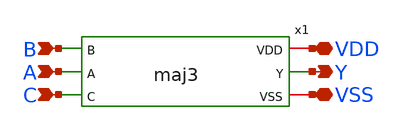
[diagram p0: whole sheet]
** sch_path: xschem/simulate.sch
**.subckt simulate A B C Y VDD VSS
*.ipin A
*.ipin B
*.ipin C
*.opin Y
*.iopin VDD
*.iopin VSS
x1 VDD B A C Y VSS maj3
**** begin user architecture code

.lib /foss/pdks/gf180mcuD/libs.tech/ngspice/sm141064.ngspice typical
.param fnoicor=1
.param sw_stat_mismatch=0
V1 VDD GND 3.3
V2 VSS GND 0
V3 A GND PULSE(0 3.3 10n 100p 100p 10n 20n)
V4 B GND PULSE(0 3.3 0 100p 100p 20n 40n)
V5 C GND PULSE(0 3.3 0 100p 100p 40n 80n)
.tran 10p 100n
.control
set filetype=ascii
run
write simulate.raw
plot v(A)-7 v(B)-3.5 v(C) v(Y)+3.5
.endc

**** end user architecture code
**.ends

* expanding   symbol:  maj3.sym # of pins=6
** sym_path: xschem/maj3.sym
** sch_path: xschem/maj3.sch
.subckt maj3 VDD B A C Y VSS
*.ipin A
*.ipin C
*.ipin B
*.opin Y
*.iopin VDD
*.iopin VSS
XM1 net1 A VDD VDD pfet_03v3 L=0.28u W=0.22u nf=1 ad='int((nf+1)/2) * W/nf * 0.18u' as='int((nf+2)/2) * W/nf * 0.18u'
+ pd='2*int((nf+1)/2) * (W/nf + 0.18u)' ps='2*int((nf+2)/2) * (W/nf + 0.18u)' nrd='0.18u / W' nrs='0.18u / W'
+ sa=0 sb=0 sd=0 m=1
XM2 X C net1 VDD pfet_03v3 L=0.28u W=0.22u nf=1 ad='int((nf+1)/2) * W/nf * 0.18u' as='int((nf+2)/2) * W/nf * 0.18u'
+ pd='2*int((nf+1)/2) * (W/nf + 0.18u)' ps='2*int((nf+2)/2) * (W/nf + 0.18u)' nrd='0.18u / W' nrs='0.18u / W'
+ sa=0 sb=0 sd=0 m=1
XM3 net2 B VDD VDD pfet_03v3 L=0.28u W=0.22u nf=1 ad='int((nf+1)/2) * W/nf * 0.18u' as='int((nf+2)/2) * W/nf * 0.18u'
+ pd='2*int((nf+1)/2) * (W/nf + 0.18u)' ps='2*int((nf+2)/2) * (W/nf + 0.18u)' nrd='0.18u / W' nrs='0.18u / W'
+ sa=0 sb=0 sd=0 m=1
XM4 net3 B VDD VDD pfet_03v3 L=0.28u W=0.22u nf=1 ad='int((nf+1)/2) * W/nf * 0.18u' as='int((nf+2)/2) * W/nf * 0.18u'
+ pd='2*int((nf+1)/2) * (W/nf + 0.18u)' ps='2*int((nf+2)/2) * (W/nf + 0.18u)' nrd='0.18u / W' nrs='0.18u / W'
+ sa=0 sb=0 sd=0 m=1
XM5 X A net3 VDD pfet_03v3 L=0.28u W=0.22u nf=1 ad='int((nf+1)/2) * W/nf * 0.18u' as='int((nf+2)/2) * W/nf * 0.18u'
+ pd='2*int((nf+1)/2) * (W/nf + 0.18u)' ps='2*int((nf+2)/2) * (W/nf + 0.18u)' nrd='0.18u / W' nrs='0.18u / W'
+ sa=0 sb=0 sd=0 m=1
XM6 X C net2 VDD pfet_03v3 L=0.28u W=0.22u nf=1 ad='int((nf+1)/2) * W/nf * 0.18u' as='int((nf+2)/2) * W/nf * 0.18u'
+ pd='2*int((nf+1)/2) * (W/nf + 0.18u)' ps='2*int((nf+2)/2) * (W/nf + 0.18u)' nrd='0.18u / W' nrs='0.18u / W'
+ sa=0 sb=0 sd=0 m=1
XM7 X C net6 VSS nfet_03v3 L=0.28u W=0.22u nf=1 ad='int((nf+1)/2) * W/nf * 0.18u' as='int((nf+2)/2) * W/nf * 0.18u'
+ pd='2*int((nf+1)/2) * (W/nf + 0.18u)' ps='2*int((nf+2)/2) * (W/nf + 0.18u)' nrd='0.18u / W' nrs='0.18u / W'
+ sa=0 sb=0 sd=0 m=1
XM8 net6 A VSS VSS nfet_03v3 L=0.28u W=0.22u nf=1 ad='int((nf+1)/2) * W/nf * 0.18u' as='int((nf+2)/2) * W/nf * 0.18u'
+ pd='2*int((nf+1)/2) * (W/nf + 0.18u)' ps='2*int((nf+2)/2) * (W/nf + 0.18u)' nrd='0.18u / W' nrs='0.18u / W'
+ sa=0 sb=0 sd=0 m=1
XM9 X C net5 VSS nfet_03v3 L=0.28u W=0.22u nf=1 ad='int((nf+1)/2) * W/nf * 0.18u' as='int((nf+2)/2) * W/nf * 0.18u'
+ pd='2*int((nf+1)/2) * (W/nf + 0.18u)' ps='2*int((nf+2)/2) * (W/nf + 0.18u)' nrd='0.18u / W' nrs='0.18u / W'
+ sa=0 sb=0 sd=0 m=1
XM10 net5 B VSS VSS nfet_03v3 L=0.28u W=0.22u nf=1 ad='int((nf+1)/2) * W/nf * 0.18u' as='int((nf+2)/2) * W/nf * 0.18u'
+ pd='2*int((nf+1)/2) * (W/nf + 0.18u)' ps='2*int((nf+2)/2) * (W/nf + 0.18u)' nrd='0.18u / W' nrs='0.18u / W'
+ sa=0 sb=0 sd=0 m=1
XM11 X A net4 VSS nfet_03v3 L=0.28u W=0.22u nf=1 ad='int((nf+1)/2) * W/nf * 0.18u' as='int((nf+2)/2) * W/nf * 0.18u'
+ pd='2*int((nf+1)/2) * (W/nf + 0.18u)' ps='2*int((nf+2)/2) * (W/nf + 0.18u)' nrd='0.18u / W' nrs='0.18u / W'
+ sa=0 sb=0 sd=0 m=1
XM12 net4 B VSS VSS nfet_03v3 L=0.28u W=0.22u nf=1 ad='int((nf+1)/2) * W/nf * 0.18u' as='int((nf+2)/2) * W/nf * 0.18u'
+ pd='2*int((nf+1)/2) * (W/nf + 0.18u)' ps='2*int((nf+2)/2) * (W/nf + 0.18u)' nrd='0.18u / W' nrs='0.18u / W'
+ sa=0 sb=0 sd=0 m=1
XM13 Y X VDD VDD pfet_03v3 L=0.28u W=0.22u nf=1 ad='int((nf+1)/2) * W/nf * 0.18u' as='int((nf+2)/2) * W/nf * 0.18u'
+ pd='2*int((nf+1)/2) * (W/nf + 0.18u)' ps='2*int((nf+2)/2) * (W/nf + 0.18u)' nrd='0.18u / W' nrs='0.18u / W'
+ sa=0 sb=0 sd=0 m=1
XM14 Y X VDD VDD pfet_03v3 L=0.28u W=0.22u nf=1 ad='int((nf+1)/2) * W/nf * 0.18u' as='int((nf+2)/2) * W/nf * 0.18u'
+ pd='2*int((nf+1)/2) * (W/nf + 0.18u)' ps='2*int((nf+2)/2) * (W/nf + 0.18u)' nrd='0.18u / W' nrs='0.18u / W'
+ sa=0 sb=0 sd=0 m=1
XM15 Y X VSS VSS nfet_03v3 L=0.28u W=0.22u nf=1 ad='int((nf+1)/2) * W/nf * 0.18u' as='int((nf+2)/2) * W/nf * 0.18u'
+ pd='2*int((nf+1)/2) * (W/nf + 0.18u)' ps='2*int((nf+2)/2) * (W/nf + 0.18u)' nrd='0.18u / W' nrs='0.18u / W'
+ sa=0 sb=0 sd=0 m=1
XM16 Y X VSS VSS nfet_03v3 L=0.28u W=0.22u nf=1 ad='int((nf+1)/2) * W/nf * 0.18u' as='int((nf+2)/2) * W/nf * 0.18u'
+ pd='2*int((nf+1)/2) * (W/nf + 0.18u)' ps='2*int((nf+2)/2) * (W/nf + 0.18u)' nrd='0.18u / W' nrs='0.18u / W'
+ sa=0 sb=0 sd=0 m=1
.ends

.end
